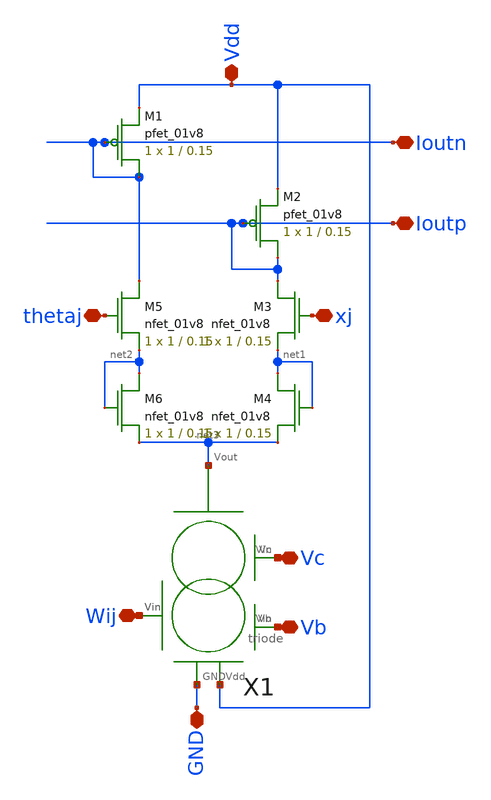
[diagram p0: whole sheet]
** sch_path: single_synapse.sch
**.subckt single_synapse Ioutn Ioutp thetaj xj Wij Vb Vc GND Vdd
*.iopin Ioutn
*.iopin Ioutp
*.iopin thetaj
*.iopin xj
*.iopin Wij
*.iopin Vb
*.iopin Vc
*.iopin GND
*.iopin Vdd
XM1 Ioutn Ioutn Vdd VDD sky130_fd_pr__pfet_01v8 L=0.15 W=1 nf=1 ad='int((nf+1)/2) * W/nf * 0.29' as='int((nf+2)/2) * W/nf * 0.29'
+ pd='2*int((nf+1)/2) * (W/nf + 0.29)' ps='2*int((nf+2)/2) * (W/nf + 0.29)' nrd='0.29 / W' nrs='0.29 / W'
+ sa=0 sb=0 sd=0 mult=1 m=1
XM2 Ioutp Ioutp Vdd VDD sky130_fd_pr__pfet_01v8 L=0.15 W=1 nf=1 ad='int((nf+1)/2) * W/nf * 0.29' as='int((nf+2)/2) * W/nf * 0.29'
+ pd='2*int((nf+1)/2) * (W/nf + 0.29)' ps='2*int((nf+2)/2) * (W/nf + 0.29)' nrd='0.29 / W' nrs='0.29 / W'
+ sa=0 sb=0 sd=0 mult=1 m=1
XM3 Ioutp xj net1 GND sky130_fd_pr__nfet_01v8 L=0.15 W=1 nf=1 ad='int((nf+1)/2) * W/nf * 0.29' as='int((nf+2)/2) * W/nf * 0.29'
+ pd='2*int((nf+1)/2) * (W/nf + 0.29)' ps='2*int((nf+2)/2) * (W/nf + 0.29)' nrd='0.29 / W' nrs='0.29 / W'
+ sa=0 sb=0 sd=0 mult=1 m=1
XM4 net1 net1 net3 GND sky130_fd_pr__nfet_01v8 L=0.15 W=1 nf=1 ad='int((nf+1)/2) * W/nf * 0.29' as='int((nf+2)/2) * W/nf * 0.29'
+ pd='2*int((nf+1)/2) * (W/nf + 0.29)' ps='2*int((nf+2)/2) * (W/nf + 0.29)' nrd='0.29 / W' nrs='0.29 / W'
+ sa=0 sb=0 sd=0 mult=1 m=1
XM5 Ioutn thetaj net2 GND sky130_fd_pr__nfet_01v8 L=0.15 W=1 nf=1 ad='int((nf+1)/2) * W/nf * 0.29' as='int((nf+2)/2) * W/nf * 0.29'
+ pd='2*int((nf+1)/2) * (W/nf + 0.29)' ps='2*int((nf+2)/2) * (W/nf + 0.29)' nrd='0.29 / W' nrs='0.29 / W'
+ sa=0 sb=0 sd=0 mult=1 m=1
XM6 net2 net2 net3 GND sky130_fd_pr__nfet_01v8 L=0.15 W=1 nf=1 ad='int((nf+1)/2) * W/nf * 0.29' as='int((nf+2)/2) * W/nf * 0.29'
+ pd='2*int((nf+1)/2) * (W/nf + 0.29)' ps='2*int((nf+2)/2) * (W/nf + 0.29)' nrd='0.29 / W' nrs='0.29 / W'
+ sa=0 sb=0 sd=0 mult=1 m=1
X1 Wij GND Vb Vc net3 Vdd triode
**.ends

* expanding   symbol:  /home/madvlsi/image_processing_final/triode.sym # of pins=9
** sym_path: triode.sym
** sch_path: triode.sch
.subckt triode Vin GND Vb Vc Vout Vdd
*.iopin Vout
*.iopin Vc
*.iopin Vb
*.iopin Vin
*.iopin GND
*.iopin Vdd
XM7 net4 net1 Vdd VDD sky130_fd_pr__pfet_01v8 L=0.15 W=1 nf=1 ad='int((nf+1)/2) * W/nf * 0.29' as='int((nf+2)/2) * W/nf * 0.29'
+ pd='2*int((nf+1)/2) * (W/nf + 0.29)' ps='2*int((nf+2)/2) * (W/nf + 0.29)' nrd='0.29 / W' nrs='0.29 / W'
+ sa=0 sb=0 sd=0 mult=1 m=1
XM6 net1 net1 Vdd VDD sky130_fd_pr__pfet_01v8 L=0.15 W=1 nf=1 ad='int((nf+1)/2) * W/nf * 0.29' as='int((nf+2)/2) * W/nf * 0.29'
+ pd='2*int((nf+1)/2) * (W/nf + 0.29)' ps='2*int((nf+2)/2) * (W/nf + 0.29)' nrd='0.29 / W' nrs='0.29 / W'
+ sa=0 sb=0 sd=0 mult=1 m=1
XM5 net1 Vc net2 GND sky130_fd_pr__nfet_01v8 L=0.15 W=1 nf=1 ad='int((nf+1)/2) * W/nf * 0.29' as='int((nf+2)/2) * W/nf * 0.29'
+ pd='2*int((nf+1)/2) * (W/nf + 0.29)' ps='2*int((nf+2)/2) * (W/nf + 0.29)' nrd='0.29 / W' nrs='0.29 / W'
+ sa=0 sb=0 sd=0 mult=1 m=1
XM1 GND net3 net2 VDD sky130_fd_pr__pfet_01v8 L=0.15 W=1 nf=1 ad='int((nf+1)/2) * W/nf * 0.29' as='int((nf+2)/2) * W/nf * 0.29'
+ pd='2*int((nf+1)/2) * (W/nf + 0.29)' ps='2*int((nf+2)/2) * (W/nf + 0.29)' nrd='0.29 / W' nrs='0.29 / W'
+ sa=0 sb=0 sd=0 mult=1 m=1
XM2 net4 Vb GND GND sky130_fd_pr__nfet_01v8 L=0.15 W=1 nf=1 ad='int((nf+1)/2) * W/nf * 0.29' as='int((nf+2)/2) * W/nf * 0.29'
+ pd='2*int((nf+1)/2) * (W/nf + 0.29)' ps='2*int((nf+2)/2) * (W/nf + 0.29)' nrd='0.29 / W' nrs='0.29 / W'
+ sa=0 sb=0 sd=0 mult=1 m=1
XM3 net3 Vin GND GND sky130_fd_pr__nfet_01v8 L=0.15 W=1 nf=1 ad='int((nf+1)/2) * W/nf * 0.29' as='int((nf+2)/2) * W/nf * 0.29'
+ pd='2*int((nf+1)/2) * (W/nf + 0.29)' ps='2*int((nf+2)/2) * (W/nf + 0.29)' nrd='0.29 / W' nrs='0.29 / W'
+ sa=0 sb=0 sd=0 mult=1 m=1
XM4 Vout net4 net3 GND sky130_fd_pr__nfet_01v8 L=0.15 W=1 nf=1 ad='int((nf+1)/2) * W/nf * 0.29' as='int((nf+2)/2) * W/nf * 0.29'
+ pd='2*int((nf+1)/2) * (W/nf + 0.29)' ps='2*int((nf+2)/2) * (W/nf + 0.29)' nrd='0.29 / W' nrs='0.29 / W'
+ sa=0 sb=0 sd=0 mult=1 m=1
.ends

.end
